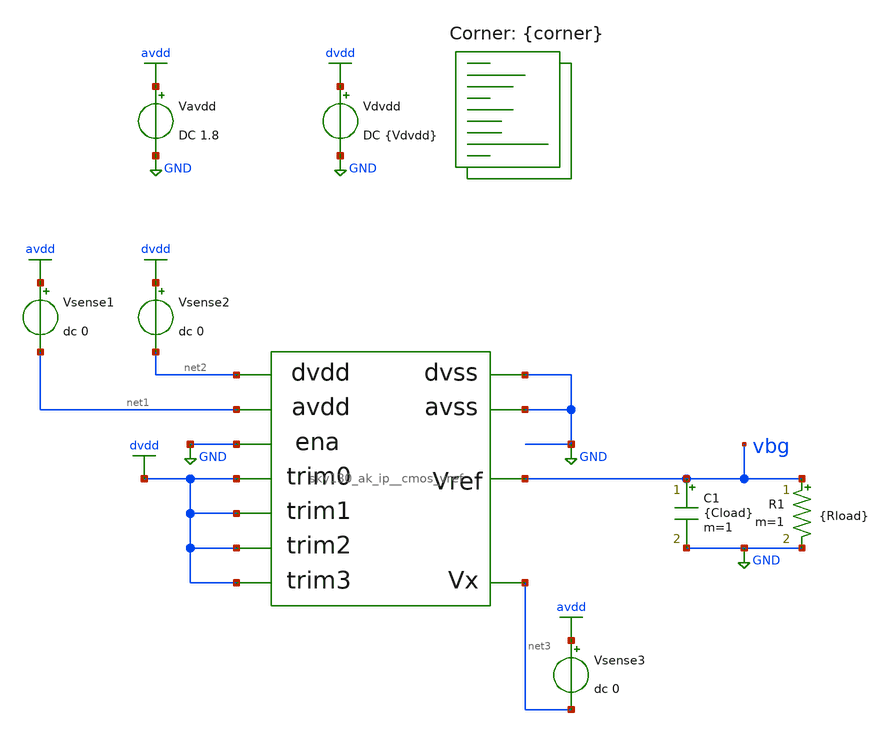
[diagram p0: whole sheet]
** sch_path: cace/tb_line_reg.sch
**.subckt tb_line_reg
Vavdd avdd GND DC 1.8
X1 net1 GND dvdd vbg net3 dvdd dvdd dvdd net2 GND GND sky130_ak_ip__cmos_vref
Vsense1 avdd net1 dc 0
Vdvdd dvdd GND DC {Vdvdd}
C1 vbg GND {Cload} m=1
Vsense2 dvdd net2 dc 0
R1 vbg GND {Rload} m=1
Vsense3 avdd net3 dc 0
**** begin user architecture code


.option warn=1
.option TEMP={temperature}
.control
save vbg
dc Vavdd {Vavdd|minimum} {Vavdd|maximum} 10m

let supply_diff = {Vavdd|maximum}-{Vavdd|minimum}
let vref_diff = maximum(vbg)-minimum(vbg)
let vref_nom = (maximum(vbg)+minimum(vbg))/2
let line_reg = vref_diff/(vref_nom*supply_diff)

echo $&line_reg > {simpath}/{filename}_{N}.data
quit
.endc


.lib $::SKYWATER_MODELS/sky130.lib.spice {corner}
**** end user architecture code
**.ends

* expanding   symbol:  /home/moduhub/work/sky130_ak_ip__cmos_vref/xschem/sky130_ak_ip__cmos_vref.sym
*+ # of pins=11
** sym_path: xschem/sky130_ak_ip__cmos_vref.sym
** sch_path: xschem/sky130_ak_ip__cmos_vref.sch
.subckt sky130_ak_ip__cmos_vref avdd avss trim0 vref vx trim1 trim2 trim3 dvdd dvss ena
*.opin vref
*.iopin avss
*.iopin avdd
*.opin vx
*.ipin trim0
*.ipin trim1
*.ipin trim2
*.ipin trim3
*.iopin dvdd
*.iopin dvss
*.iopin avdd
*.ipin ena
XM3 net1 net3 vx GND sky130_fd_pr__nfet_g5v0d10v5 L=1 W=100 nf=5 ad='int((nf+1)/2) * W/nf * 0.29' as='int((nf+2)/2) * W/nf * 0.29'
+ pd='2*int((nf+1)/2) * (W/nf + 0.29)' ps='2*int((nf+2)/2) * (W/nf + 0.29)' nrd='0.29 / W' nrs='0.29 / W'
+ sa=0 sb=0 sd=0 mult=1 m=1
XM4 net2 net3 avss GND sky130_fd_pr__nfet_g5v0d10v5 L=1 W=5 nf=1 ad='int((nf+1)/2) * W/nf * 0.29' as='int((nf+2)/2) * W/nf * 0.29'
+ pd='2*int((nf+1)/2) * (W/nf + 0.29)' ps='2*int((nf+2)/2) * (W/nf + 0.29)' nrd='0.29 / W' nrs='0.29 / W'
+ sa=0 sb=0 sd=0 mult=1 m=1
XM5 net4 vref net1 GND sky130_fd_pr__nfet_g5v0d10v5 L=10 W=10 nf=1 ad='int((nf+1)/2) * W/nf * 0.29' as='int((nf+2)/2) * W/nf * 0.29'
+ pd='2*int((nf+1)/2) * (W/nf + 0.29)' ps='2*int((nf+2)/2) * (W/nf + 0.29)' nrd='0.29 / W' nrs='0.29 / W'
+ sa=0 sb=0 sd=0 mult=1 m=1
XM6 net3 vref net2 GND sky130_fd_pr__nfet_g5v0d10v5 L=10 W=10 nf=1 ad='int((nf+1)/2) * W/nf * 0.29' as='int((nf+2)/2) * W/nf * 0.29'
+ pd='2*int((nf+1)/2) * (W/nf + 0.29)' ps='2*int((nf+2)/2) * (W/nf + 0.29)' nrd='0.29 / W' nrs='0.29 / W'
+ sa=0 sb=0 sd=0 mult=1 m=1
XM7 net4 net4 avdd_ena avdd sky130_fd_pr__pfet_g5v0d10v5 L=10 W=5 nf=1 ad='int((nf+1)/2) * W/nf * 0.29'
+ as='int((nf+2)/2) * W/nf * 0.29' pd='2*int((nf+1)/2) * (W/nf + 0.29)' ps='2*int((nf+2)/2) * (W/nf + 0.29)'
+ nrd='0.29 / W' nrs='0.29 / W' sa=0 sb=0 sd=0 mult=1 m=1
XM8 net3 net4 avdd_ena avdd sky130_fd_pr__pfet_g5v0d10v5 L=10 W=5 nf=1 ad='int((nf+1)/2) * W/nf * 0.29'
+ as='int((nf+2)/2) * W/nf * 0.29' pd='2*int((nf+1)/2) * (W/nf + 0.29)' ps='2*int((nf+2)/2) * (W/nf + 0.29)'
+ nrd='0.29 / W' nrs='0.29 / W' sa=0 sb=0 sd=0 mult=1 m=1
XM9 vref net4 avdd_ena avdd sky130_fd_pr__pfet_g5v0d10v5 L=10 W=50 nf=1 ad='int((nf+1)/2) * W/nf * 0.29'
+ as='int((nf+2)/2) * W/nf * 0.29' pd='2*int((nf+1)/2) * (W/nf + 0.29)' ps='2*int((nf+2)/2) * (W/nf + 0.29)'
+ nrd='0.29 / W' nrs='0.29 / W' sa=0 sb=0 sd=0 mult=1 m=1
XM10 net5 net3 avss GND sky130_fd_pr__nfet_g5v0d10v5 L=1 W=5 nf=1 ad='int((nf+1)/2) * W/nf * 0.29' as='int((nf+2)/2) * W/nf * 0.29'
+ pd='2*int((nf+1)/2) * (W/nf + 0.29)' ps='2*int((nf+2)/2) * (W/nf + 0.29)' nrd='0.29 / W' nrs='0.29 / W'
+ sa=0 sb=0 sd=0 mult=1 m=1
XM11 net4 net5 avss GND sky130_fd_pr__nfet_g5v0d10v5 L=1 W=5 nf=1 ad='int((nf+1)/2) * W/nf * 0.29' as='int((nf+2)/2) * W/nf * 0.29'
+ pd='2*int((nf+1)/2) * (W/nf + 0.29)' ps='2*int((nf+2)/2) * (W/nf + 0.29)' nrd='0.29 / W' nrs='0.29 / W'
+ sa=0 sb=0 sd=0 mult=1 m=1
XC1 avdd_ena net5 sky130_fd_pr__cap_mim_m3_1 W=5 L=5 MF=1 m=1
XM12 vref net4 net9 avdd sky130_fd_pr__pfet_g5v0d10v5 L=10 W=1 nf=1 ad='int((nf+1)/2) * W/nf * 0.29'
+ as='int((nf+2)/2) * W/nf * 0.29' pd='2*int((nf+1)/2) * (W/nf + 0.29)' ps='2*int((nf+2)/2) * (W/nf + 0.29)'
+ nrd='0.29 / W' nrs='0.29 / W' sa=0 sb=0 sd=0 mult=1 m=1
XM13 vref net4 net8 avdd sky130_fd_pr__pfet_g5v0d10v5 L=10 W=2 nf=1 ad='int((nf+1)/2) * W/nf * 0.29'
+ as='int((nf+2)/2) * W/nf * 0.29' pd='2*int((nf+1)/2) * (W/nf + 0.29)' ps='2*int((nf+2)/2) * (W/nf + 0.29)'
+ nrd='0.29 / W' nrs='0.29 / W' sa=0 sb=0 sd=0 mult=1 m=1
XM14 net9 trim0 avdd_ena dvdd sky130_fd_pr__pfet_g5v0d10v5 L=0.15 W=1 nf=1 ad='int((nf+1)/2) * W/nf * 0.29'
+ as='int((nf+2)/2) * W/nf * 0.29' pd='2*int((nf+1)/2) * (W/nf + 0.29)' ps='2*int((nf+2)/2) * (W/nf + 0.29)'
+ nrd='0.29 / W' nrs='0.29 / W' sa=0 sb=0 sd=0 mult=1 m=1
XM15 net8 trim1 avdd_ena dvdd sky130_fd_pr__pfet_g5v0d10v5 L=0.15 W=1 nf=1 ad='int((nf+1)/2) * W/nf * 0.29'
+ as='int((nf+2)/2) * W/nf * 0.29' pd='2*int((nf+1)/2) * (W/nf + 0.29)' ps='2*int((nf+2)/2) * (W/nf + 0.29)'
+ nrd='0.29 / W' nrs='0.29 / W' sa=0 sb=0 sd=0 mult=1 m=1
XM16 vref net4 net7 avdd sky130_fd_pr__pfet_g5v0d10v5 L=10 W=4 nf=1 ad='int((nf+1)/2) * W/nf * 0.29'
+ as='int((nf+2)/2) * W/nf * 0.29' pd='2*int((nf+1)/2) * (W/nf + 0.29)' ps='2*int((nf+2)/2) * (W/nf + 0.29)'
+ nrd='0.29 / W' nrs='0.29 / W' sa=0 sb=0 sd=0 mult=1 m=1
XM17 net7 trim2 avdd_ena dvdd sky130_fd_pr__pfet_g5v0d10v5 L=0.15 W=1 nf=1 ad='int((nf+1)/2) * W/nf * 0.29'
+ as='int((nf+2)/2) * W/nf * 0.29' pd='2*int((nf+1)/2) * (W/nf + 0.29)' ps='2*int((nf+2)/2) * (W/nf + 0.29)'
+ nrd='0.29 / W' nrs='0.29 / W' sa=0 sb=0 sd=0 mult=1 m=1
XM18 vref net4 net6 avdd sky130_fd_pr__pfet_g5v0d10v5 L=10 W=8 nf=1 ad='int((nf+1)/2) * W/nf * 0.29'
+ as='int((nf+2)/2) * W/nf * 0.29' pd='2*int((nf+1)/2) * (W/nf + 0.29)' ps='2*int((nf+2)/2) * (W/nf + 0.29)'
+ nrd='0.29 / W' nrs='0.29 / W' sa=0 sb=0 sd=0 mult=1 m=1
XM19 net6 trim3 avdd_ena dvdd sky130_fd_pr__pfet_g5v0d10v5 L=0.15 W=1 nf=1 ad='int((nf+1)/2) * W/nf * 0.29'
+ as='int((nf+2)/2) * W/nf * 0.29' pd='2*int((nf+1)/2) * (W/nf + 0.29)' ps='2*int((nf+2)/2) * (W/nf + 0.29)'
+ nrd='0.29 / W' nrs='0.29 / W' sa=0 sb=0 sd=0 mult=1 m=1
XM1 vx vref avss GND sky130_fd_pr__nfet_g5v0d10v5 L=10 W=2.5 nf=1 ad='int((nf+1)/2) * W/nf * 0.29' as='int((nf+2)/2) * W/nf * 0.29'
+ pd='2*int((nf+1)/2) * (W/nf + 0.29)' ps='2*int((nf+2)/2) * (W/nf + 0.29)' nrd='0.29 / W' nrs='0.29 / W'
+ sa=0 sb=0 sd=0 mult=1 m=1
XM2 vref vref vx GND sky130_fd_pr__nfet_g5v0d10v5 L=10 W=2 nf=1 ad='int((nf+1)/2) * W/nf * 0.29' as='int((nf+2)/2) * W/nf * 0.29'
+ pd='2*int((nf+1)/2) * (W/nf + 0.29)' ps='2*int((nf+2)/2) * (W/nf + 0.29)' nrd='0.29 / W' nrs='0.29 / W'
+ sa=0 sb=0 sd=0 mult=1 m=1
XM20 avdd_ena ena avdd dvdd sky130_fd_pr__pfet_g5v0d10v5 L=0.3 W=5 nf=1 ad='int((nf+1)/2) * W/nf * 0.29'
+ as='int((nf+2)/2) * W/nf * 0.29' pd='2*int((nf+1)/2) * (W/nf + 0.29)' ps='2*int((nf+2)/2) * (W/nf + 0.29)'
+ nrd='0.29 / W' nrs='0.29 / W' sa=0 sb=0 sd=0 mult=1 m=1
.ends

.GLOBAL avdd
.GLOBAL GND
.GLOBAL dvdd
.end
